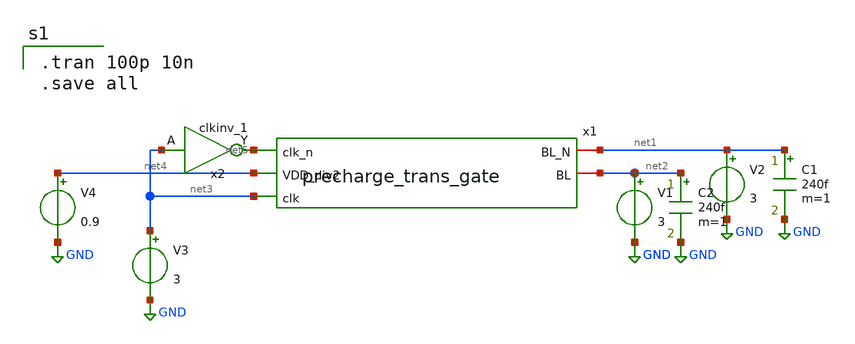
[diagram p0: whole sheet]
** sch_path: analog/schematics/trans_gate_tb.sch
**.subckt trans_gate_tb
x1 net5 net1 net2 net4 net3 precharge_trans_gate
V1 net2 GND 3
V2 net1 GND 3
V3 net3 GND 3
x2 net3 VGND VNB VPB VPWR net5 sky130_fd_sc_hd__clkinv_1
V4 net4 GND 0.9
C1 net1 GND 240f m=1
C2 net2 GND 240f m=1
**** begin user architecture code

.tran 100p 10n
.save all

**** end user architecture code
**.ends

* expanding   symbol:  precharge_trans_gate.sym # of pins=5
** sym_path: analog/schematics/precharge_trans_gate.sym
** sch_path: analog/schematics/precharge_trans_gate.sch
.subckt precharge_trans_gate clk_n BL_N BL VDD_div2 clk
*.ipin VDD_div2
*.ipin clk_n
*.ipin clk
*.iopin BL
*.iopin BL_N
XM1 VDD_div2 clk BL GND sky130_fd_pr__nfet_01v8 L=0.15 W=2 nf=1 ad='int((nf+1)/2) * W/nf * 0.29' as='int((nf+2)/2) * W/nf * 0.29'
+ pd='2*int((nf+1)/2) * (W/nf + 0.29)' ps='2*int((nf+2)/2) * (W/nf + 0.29)' nrd='0.29 / W' nrs='0.29 / W'
+ sa=0 sb=0 sd=0 mult=1 m=1
XM3 BL_N clk VDD_div2 GND sky130_fd_pr__nfet_01v8 L=0.15 W=2 nf=1 ad='int((nf+1)/2) * W/nf * 0.29' as='int((nf+2)/2) * W/nf * 0.29'
+ pd='2*int((nf+1)/2) * (W/nf + 0.29)' ps='2*int((nf+2)/2) * (W/nf + 0.29)' nrd='0.29 / W' nrs='0.29 / W'
+ sa=0 sb=0 sd=0 mult=1 m=1
XM2 VDD_div2 clk_n BL BL sky130_fd_pr__pfet_01v8 L=0.15 W=3 nf=1 ad='int((nf+1)/2) * W/nf * 0.29' as='int((nf+2)/2) * W/nf * 0.29'
+ pd='2*int((nf+1)/2) * (W/nf + 0.29)' ps='2*int((nf+2)/2) * (W/nf + 0.29)' nrd='0.29 / W' nrs='0.29 / W'
+ sa=0 sb=0 sd=0 mult=1 m=1
XM4 BL_N clk_n VDD_div2 VDD_div2 sky130_fd_pr__pfet_01v8 L=0.15 W=3 nf=1 ad='int((nf+1)/2) * W/nf * 0.29'
+ as='int((nf+2)/2) * W/nf * 0.29' pd='2*int((nf+1)/2) * (W/nf + 0.29)' ps='2*int((nf+2)/2) * (W/nf + 0.29)'
+ nrd='0.29 / W' nrs='0.29 / W' sa=0 sb=0 sd=0 mult=1 m=1
XM5 BL clk BL_N GND sky130_fd_pr__nfet_01v8 L=0.15 W=1 nf=1 ad='int((nf+1)/2) * W/nf * 0.29' as='int((nf+2)/2) * W/nf * 0.29'
+ pd='2*int((nf+1)/2) * (W/nf + 0.29)' ps='2*int((nf+2)/2) * (W/nf + 0.29)' nrd='0.29 / W' nrs='0.29 / W'
+ sa=0 sb=0 sd=0 mult=1 m=1
.ends

.GLOBAL GND
.end
